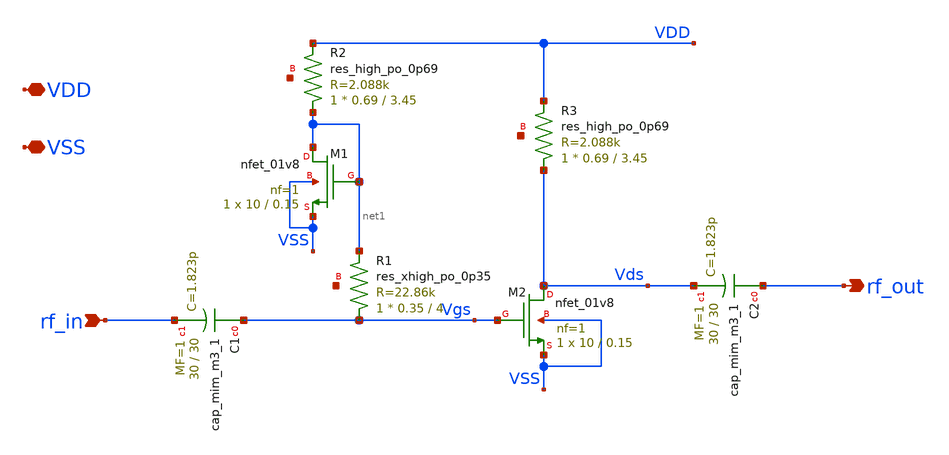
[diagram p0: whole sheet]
** sch_path: xschem/degenerated_lna.sch
**.subckt degenerated_lna VDD VSS rf_in rf_out
*.iopin VDD
*.iopin VSS
*.ipin rf_in
*.opin rf_out
XM1 net1 net1 VSS VSS sky130_fd_pr__nfet_01v8 L=0.15 W=10 nf=1 ad='int((nf+1)/2) * W/nf * 0.29' as='int((nf+2)/2) * W/nf * 0.29'
+ pd='2*int((nf+1)/2) * (W/nf + 0.29)' ps='2*int((nf+2)/2) * (W/nf + 0.29)' nrd='0.29 / W' nrs='0.29 / W'
+ sa=0 sb=0 sd=0 mult=1 m=1
XM2 Vds Vgs VSS VSS sky130_fd_pr__nfet_01v8 L=0.15 W=10 nf=1 ad='int((nf+1)/2) * W/nf * 0.29' as='int((nf+2)/2) * W/nf * 0.29'
+ pd='2*int((nf+1)/2) * (W/nf + 0.29)' ps='2*int((nf+2)/2) * (W/nf + 0.29)' nrd='0.29 / W' nrs='0.29 / W'
+ sa=0 sb=0 sd=0 mult=1 m=1
XC1 Vgs rf_in sky130_fd_pr__cap_mim_m3_1 W=30 L=30 MF=1 m=1
XC2 rf_out Vds sky130_fd_pr__cap_mim_m3_1 W=30 L=30 MF=1 m=1
XR1 Vgs net1 net2 sky130_fd_pr__res_xhigh_po_0p35 L=4 mult=1 m=1
XR2 net1 VDD net3 sky130_fd_pr__res_high_po_0p69 L=3.45 mult=1 m=1
XR3 Vds VDD net4 sky130_fd_pr__res_high_po_0p69 L=3.45 mult=1 m=1
**.ends
.end
